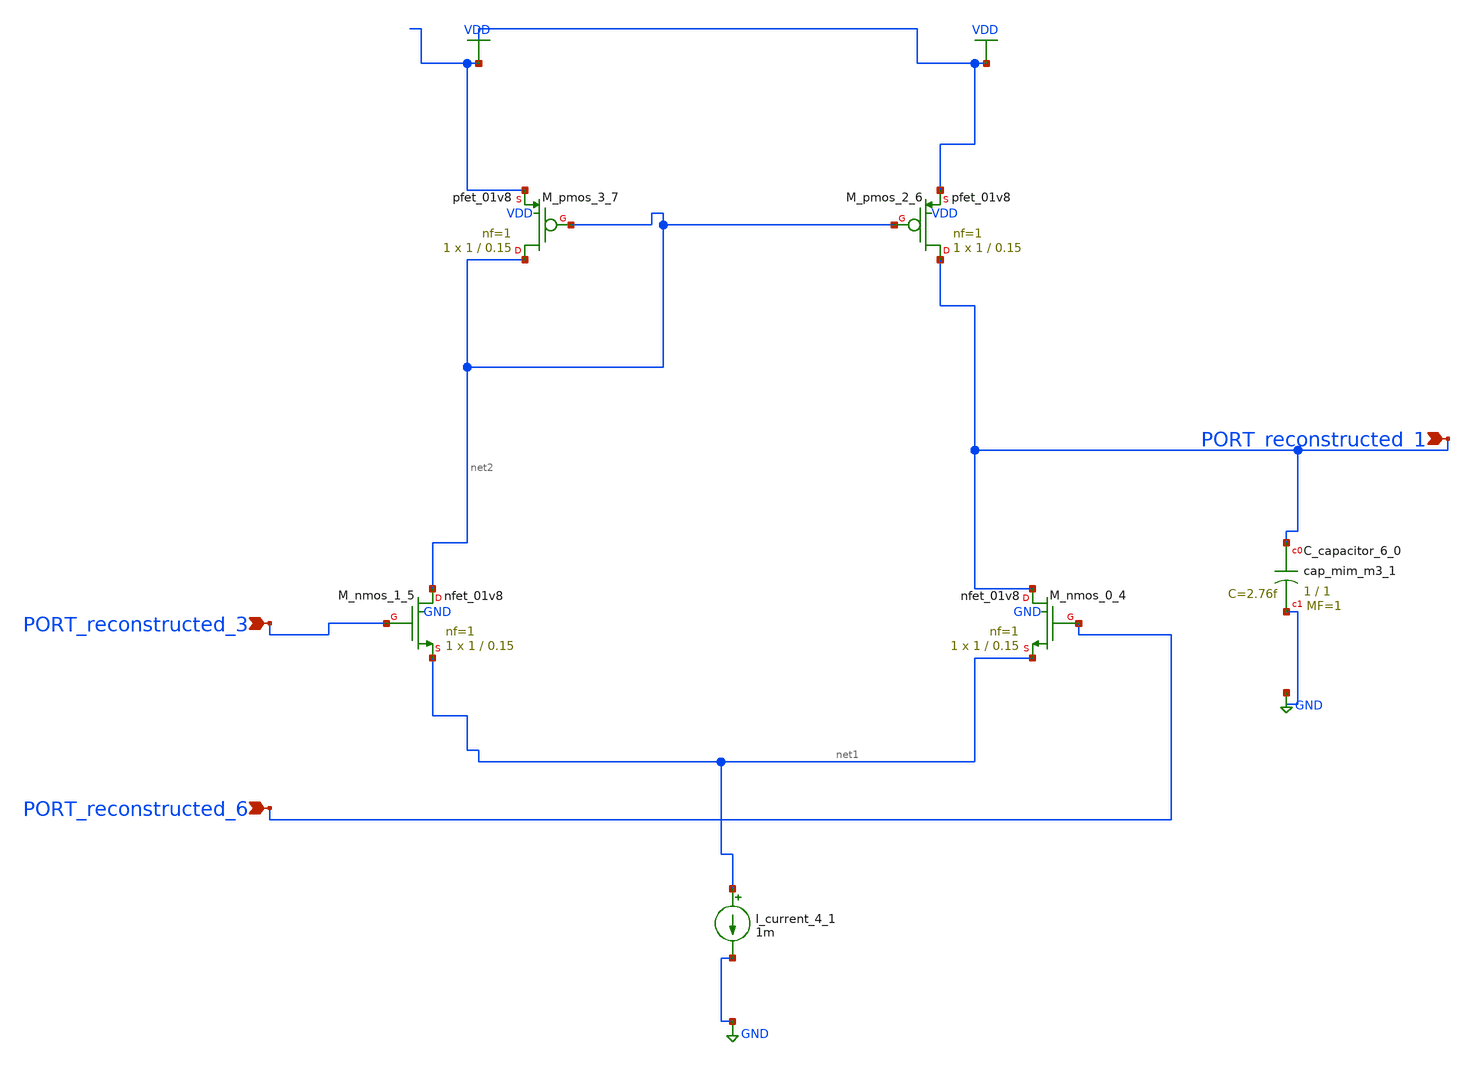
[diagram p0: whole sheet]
** sch_path: schematics/SchemGen/10_11648_j_ajpa_20241201_12_02_003.sch
**.subckt 10_11648_j_ajpa_20241201_12_02_003 PORT_reconstructed_6 PORT_reconstructed_1
*+ PORT_reconstructed_3
*.ipin PORT_reconstructed_6
*.ipin PORT_reconstructed_1
*.ipin PORT_reconstructed_3
XC_capacitor_6_0 PORT_reconstructed_1 GND sky130_fd_pr__cap_mim_m3_1 W=1 L=1 MF=1 m=1
I_current_4_1 net1 GND 1m
XM_nmos_0_4 PORT_reconstructed_1 PORT_reconstructed_6 net1 GND sky130_fd_pr__nfet_01v8 L=0.15 W=1 nf=1
+ ad='int((1 + 1)/2) * 1 / 1 * 0.29' as='int((1 + 2)/2) * 1 / 1 * 0.29' pd='2*int((1 + 1)/2) * (1 / 1 + 0.29)'
+ ps='2*int((1 + 2)/2) * (1 / 1 + 0.29)' nrd='0.29 / 1 ' nrs='0.29 / 1 ' sa=0 sb=0 sd=0 mult=1 m=1
XM_nmos_1_5 net2 PORT_reconstructed_3 net1 GND sky130_fd_pr__nfet_01v8 L=0.15 W=1 nf=1 ad='int((1 + 1)/2) * 1 / 1 * 0.29'
+ as='int((1 + 2)/2) * 1 / 1 * 0.29' pd='2*int((1 + 1)/2) * (1 / 1 + 0.29)' ps='2*int((1 + 2)/2) * (1 / 1 + 0.29)'
+ nrd='0.29 / 1 ' nrs='0.29 / 1 ' sa=0 sb=0 sd=0 mult=1 m=1
XM_pmos_2_6 PORT_reconstructed_1 net2 VDD VDD sky130_fd_pr__pfet_01v8 L=0.15 W=1 nf=1 ad='int((1 + 1)/2) * 1 / 1 * 0.29'
+ as='int((1 + 2)/2) * 1 / 1 * 0.29' pd='2*int((1 + 1)/2) * (1 / 1 + 0.29)' ps='2*int((1 + 2)/2) * (1 / 1 + 0.29)'
+ nrd='0.29 / 1 ' nrs='0.29 / 1 ' sa=0 sb=0 sd=0 mult=1 m=1
XM_pmos_3_7 net2 net2 VDD VDD sky130_fd_pr__pfet_01v8 L=0.15 W=1 nf=1 ad='int((1 + 1)/2) * 1 / 1 * 0.29'
+ as='int((1 + 2)/2) * 1 / 1 * 0.29' pd='2*int((1 + 1)/2) * (1 / 1 + 0.29)' ps='2*int((1 + 2)/2) * (1 / 1 + 0.29)'
+ nrd='0.29 / 1 ' nrs='0.29 / 1 ' sa=0 sb=0 sd=0 mult=1 m=1
**.ends
.GLOBAL GND
.GLOBAL VDD
.end
